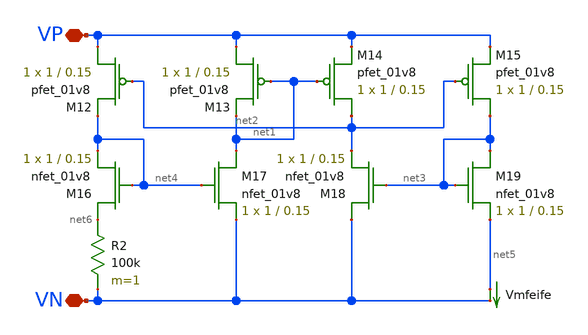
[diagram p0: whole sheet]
** sch_path: schematics/bias_generator.sch
**.subckt bias_generator VP VN
*.iopin VP
*.iopin VN
XM12 VP net2 net4 VDD sky130_fd_pr__pfet_01v8 L=0.15 W=1 nf=1 ad='int((nf+1)/2) * W/nf * 0.29' as='int((nf+2)/2) * W/nf * 0.29'
+ pd='2*int((nf+1)/2) * (W/nf + 0.29)' ps='2*int((nf+2)/2) * (W/nf + 0.29)' nrd='0.29 / W' nrs='0.29 / W'
+ sa=0 sb=0 sd=0 mult=1 m=1
XM13 VP net1 net1 VDD sky130_fd_pr__pfet_01v8 L=0.15 W=1 nf=1 ad='int((nf+1)/2) * W/nf * 0.29' as='int((nf+2)/2) * W/nf * 0.29'
+ pd='2*int((nf+1)/2) * (W/nf + 0.29)' ps='2*int((nf+2)/2) * (W/nf + 0.29)' nrd='0.29 / W' nrs='0.29 / W'
+ sa=0 sb=0 sd=0 mult=1 m=1
XM14 net2 net1 VP VDD sky130_fd_pr__pfet_01v8 L=0.15 W=1 nf=1 ad='int((nf+1)/2) * W/nf * 0.29' as='int((nf+2)/2) * W/nf * 0.29'
+ pd='2*int((nf+1)/2) * (W/nf + 0.29)' ps='2*int((nf+2)/2) * (W/nf + 0.29)' nrd='0.29 / W' nrs='0.29 / W'
+ sa=0 sb=0 sd=0 mult=1 m=1
XM15 net3 net2 VP VDD sky130_fd_pr__pfet_01v8 L=0.15 W=1 nf=1 ad='int((nf+1)/2) * W/nf * 0.29' as='int((nf+2)/2) * W/nf * 0.29'
+ pd='2*int((nf+1)/2) * (W/nf + 0.29)' ps='2*int((nf+2)/2) * (W/nf + 0.29)' nrd='0.29 / W' nrs='0.29 / W'
+ sa=0 sb=0 sd=0 mult=1 m=1
XM16 net6 net4 net4 GND sky130_fd_pr__nfet_01v8 L=0.15 W=1 nf=1 ad='int((nf+1)/2) * W/nf * 0.29' as='int((nf+2)/2) * W/nf * 0.29'
+ pd='2*int((nf+1)/2) * (W/nf + 0.29)' ps='2*int((nf+2)/2) * (W/nf + 0.29)' nrd='0.29 / W' nrs='0.29 / W'
+ sa=0 sb=0 sd=0 mult=1 m=1
XM17 net1 net4 VN GND sky130_fd_pr__nfet_01v8 L=0.15 W=1 nf=1 ad='int((nf+1)/2) * W/nf * 0.29' as='int((nf+2)/2) * W/nf * 0.29'
+ pd='2*int((nf+1)/2) * (W/nf + 0.29)' ps='2*int((nf+2)/2) * (W/nf + 0.29)' nrd='0.29 / W' nrs='0.29 / W'
+ sa=0 sb=0 sd=0 mult=1 m=1
XM18 VN net3 net2 GND sky130_fd_pr__nfet_01v8 L=0.15 W=1 nf=1 ad='int((nf+1)/2) * W/nf * 0.29' as='int((nf+2)/2) * W/nf * 0.29'
+ pd='2*int((nf+1)/2) * (W/nf + 0.29)' ps='2*int((nf+2)/2) * (W/nf + 0.29)' nrd='0.29 / W' nrs='0.29 / W'
+ sa=0 sb=0 sd=0 mult=1 m=1
XM19 net3 net3 net5 GND sky130_fd_pr__nfet_01v8 L=0.15 W=1 nf=1 ad='int((nf+1)/2) * W/nf * 0.29' as='int((nf+2)/2) * W/nf * 0.29'
+ pd='2*int((nf+1)/2) * (W/nf + 0.29)' ps='2*int((nf+2)/2) * (W/nf + 0.29)' nrd='0.29 / W' nrs='0.29 / W'
+ sa=0 sb=0 sd=0 mult=1 m=1
R2 net6 VN 100k m=1
Vmfeife net5 VN 0
.save i(vmfeife)
**.ends
.end
